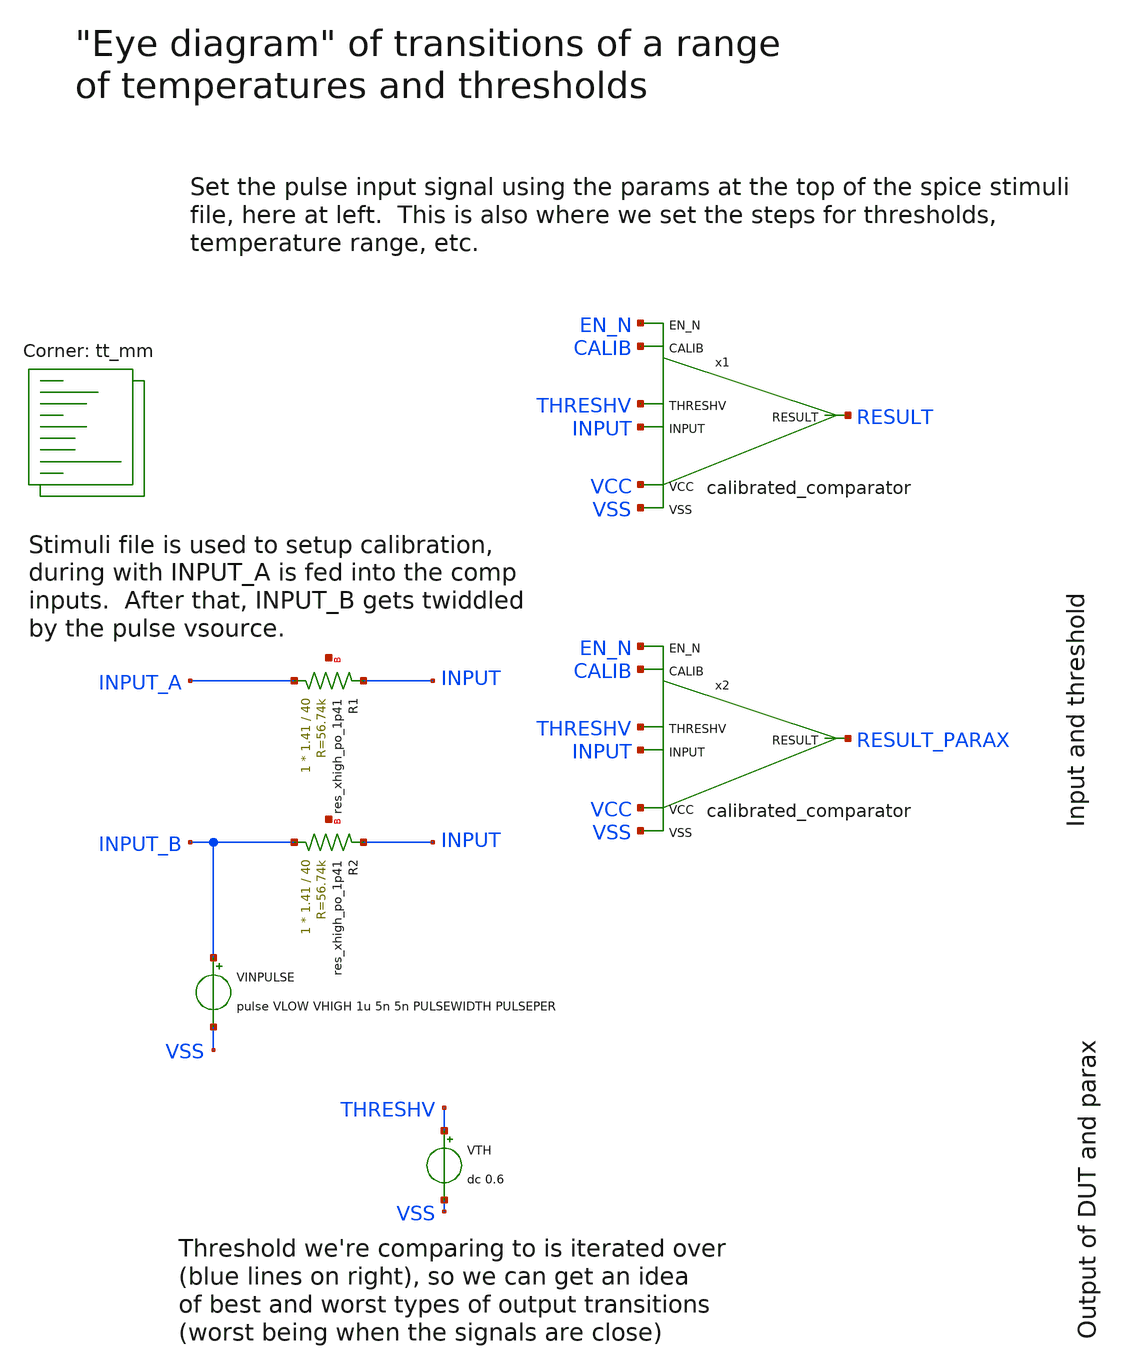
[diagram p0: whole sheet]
** sch_path: xschem/tb_calibrated_comparator_eyediag.sch
**.subckt tb_calibrated_comparator_eyediag
x1 VCC VSS INPUT THRESHV RESULT CALIB EN_N calibrated_comparator
x2 VCC VSS INPUT THRESHV RESULT_PARAX CALIB EN_N calibrated_comparator
XR1 INPUT_A INPUT net1 sky130_fd_pr__res_xhigh_po_1p41 L=40 mult=1 m=1
XR2 INPUT_B INPUT net2 sky130_fd_pr__res_xhigh_po_1p41 L=40 mult=1 m=1
VINPULSE INPUT_B VSS pulse VLOW VHIGH 1u 5n 5n PULSEWIDTH PULSEPER
VTH THRESHV VSS dc 0.6
**** begin user architecture code
.lib $::SKYWATER_MODELS/sky130.lib.spice tt_mm




* Threshold pulse signals parms
.param VLOW = -0.2
.param VHIGH =2.2
.param PULSEWIDTH = 100n
.param PULSEPER = 200n



** this experimental option enables mos model bin
** selection based on W/NF instead of W
.option chgtol=4e-16 method=gear

.param VCCGAUSS = agauss(1.8, 0.05, 1)
.param VCC = 'VCCGAUSS'
** use following line to remove VCC variations
* .param VCC = 1.8
.param VDLGAUSS = agauss(0.9, 0.23, 1)
.param VDL = VDLGAUSS
** use following line to remove input common mode variations
* .param VDL =  1.4
.param TEMPGAUSS = agauss(40, 30, 1)
.option temp = 'TEMPGAUSS'
** use following line to remove temperature variations
* .option temp = 25
.param DELTA = 0.002


* our calibration stage/setup
.include stimuli_tb_calibrated_comparator_eyediag.cir


.control
  setseed  8
  reset
  let run = 1
  let pw = 50n
  let pp = 100n
  let vthresh = 0.01
  save all
  op
  write tb_calibrated_comparator_eyediag.raw
  reset
  set appendwrite
  dowhile vthresh <= 1.6

   alter VTH vthresh
   dowhile run < = 3
    save all
    let pw = pw * 2
    let pp = pw * 2
    * alter VINPULSE PW = pw
    * alter VINPULSE PER = pp
    tran 1n 3200n uic
    write tb_calibrated_comparator_eyediag.raw
    let run = run + 1
    reset
   end
   let vthresh = vthresh + 0.05
  end
  quit 0
.endc


**** end user architecture code
**.ends
.end
